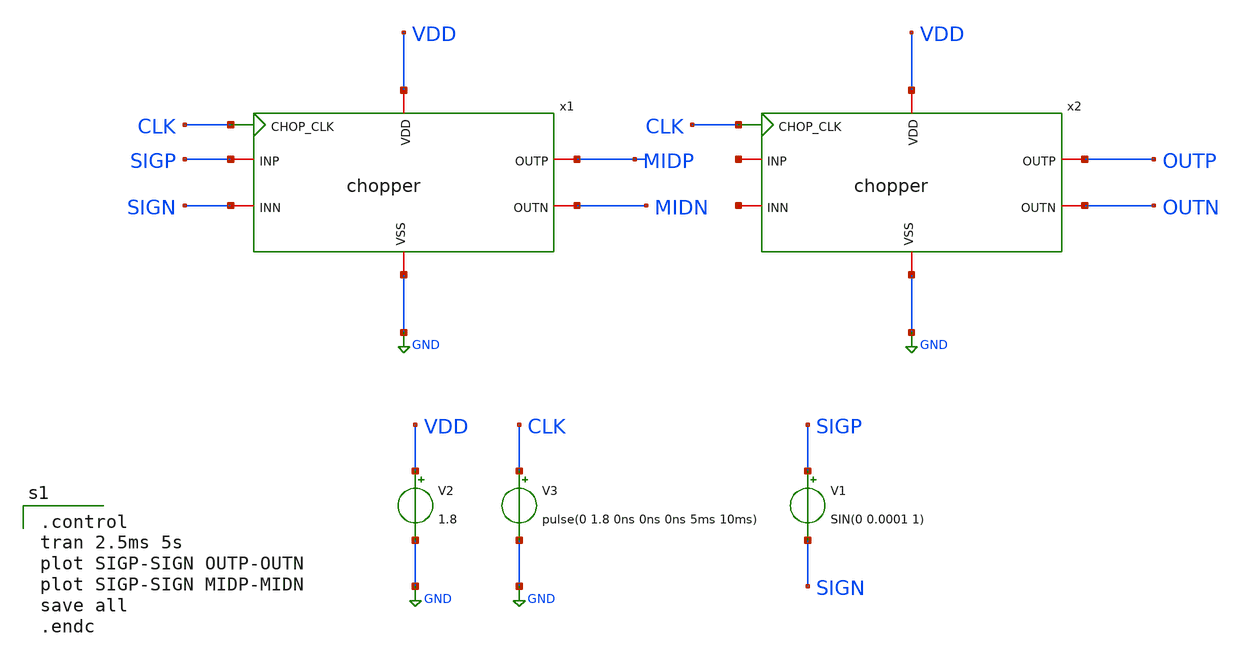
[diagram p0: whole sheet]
** sch_path: opamp_lna/chopper_tb.sch
**.subckt chopper_tb
x1 GND VDD MIDP SIGP CLK MIDN SIGN chopper
V1 SIGP SIGN SIN(0 0.0001 1)
V2 VDD GND 1.8
V3 CLK GND pulse(0 1.8 0ns 0ns 0ns 5ms 10ms)
x2 GND VDD OUTP net1 CLK OUTN net2 chopper
**** begin user architecture code

** opencircuitdesign pdks install
.lib $::SKYWATER_MODELS/sky130.lib.spice tt
.include $::SKYWATER_STDCELLS/sky130_fd_sc_hd.spice


.control
tran 2.5ms 5s
plot SIGP-SIGN OUTP-OUTN
plot SIGP-SIGN MIDP-MIDN
save all
.endc

**** end user architecture code
**.ends

* expanding   symbol:  chopper.sym # of pins=7
** sym_path: opamp_lna/chopper.sym
** sch_path: opamp_lna/chopper.sch
.subckt chopper VSS VDD OUTP INP CHOP_CLK OUTN INN
*.ipin CHOP_CLK
*.iopin INP
*.iopin INN
*.iopin OUTP
*.iopin OUTN
*.iopin VSS
*.iopin VDD
x5 CHOP_CLK VSS VNB VPB VDD net2 sky130_fd_sc_hd__clkbuf_2
x1 CHOP_CLK VGND VNB VPB VPWR net1 sky130_fd_sc_hd__clkinv_2
x2 net1 VSS VNB VPB VDD SWB sky130_fd_sc_hd__clkinv_8
x3 net2 VSS VNB VPB VDD SW sky130_fd_sc_hd__clkinv_8
XM5 INP SWB OUTN VSS sky130_fd_pr__nfet_01v8 L=0.15 W=1 nf=1 ad='int((nf+1)/2) * W/nf * 0.29' as='int((nf+2)/2) * W/nf * 0.29'
+ pd='2*int((nf+1)/2) * (W/nf + 0.29)' ps='2*int((nf+2)/2) * (W/nf + 0.29)' nrd='0.29 / W' nrs='0.29 / W'
+ sa=0 sb=0 sd=0 mult=1 m=1
XM6 OUTN SW INP VDD sky130_fd_pr__pfet_01v8 L=0.15 W=1 nf=1 ad='int((nf+1)/2) * W/nf * 0.29' as='int((nf+2)/2) * W/nf * 0.29'
+ pd='2*int((nf+1)/2) * (W/nf + 0.29)' ps='2*int((nf+2)/2) * (W/nf + 0.29)' nrd='0.29 / W' nrs='0.29 / W'
+ sa=0 sb=0 sd=0 mult=1 m=1
XM7 INP SW OUTP VSS sky130_fd_pr__nfet_01v8 L=0.15 W=8 nf=1 ad='int((nf+1)/2) * W/nf * 0.29' as='int((nf+2)/2) * W/nf * 0.29'
+ pd='2*int((nf+1)/2) * (W/nf + 0.29)' ps='2*int((nf+2)/2) * (W/nf + 0.29)' nrd='0.29 / W' nrs='0.29 / W'
+ sa=0 sb=0 sd=0 mult=1 m=1
XM8 OUTP SWB INP VDD sky130_fd_pr__pfet_01v8 L=0.15 W=8 nf=1 ad='int((nf+1)/2) * W/nf * 0.29' as='int((nf+2)/2) * W/nf * 0.29'
+ pd='2*int((nf+1)/2) * (W/nf + 0.29)' ps='2*int((nf+2)/2) * (W/nf + 0.29)' nrd='0.29 / W' nrs='0.29 / W'
+ sa=0 sb=0 sd=0 mult=1 m=1
XM9 INN SW OUTN VSS sky130_fd_pr__nfet_01v8 L=0.15 W=8 nf=1 ad='int((nf+1)/2) * W/nf * 0.29' as='int((nf+2)/2) * W/nf * 0.29'
+ pd='2*int((nf+1)/2) * (W/nf + 0.29)' ps='2*int((nf+2)/2) * (W/nf + 0.29)' nrd='0.29 / W' nrs='0.29 / W'
+ sa=0 sb=0 sd=0 mult=1 m=1
XM10 OUTN SWB INN VDD sky130_fd_pr__pfet_01v8 L=0.15 W=8 nf=1 ad='int((nf+1)/2) * W/nf * 0.29' as='int((nf+2)/2) * W/nf * 0.29'
+ pd='2*int((nf+1)/2) * (W/nf + 0.29)' ps='2*int((nf+2)/2) * (W/nf + 0.29)' nrd='0.29 / W' nrs='0.29 / W'
+ sa=0 sb=0 sd=0 mult=1 m=1
XM11 INN SWB OUTP VSS sky130_fd_pr__nfet_01v8 L=0.15 W=8 nf=1 ad='int((nf+1)/2) * W/nf * 0.29' as='int((nf+2)/2) * W/nf * 0.29'
+ pd='2*int((nf+1)/2) * (W/nf + 0.29)' ps='2*int((nf+2)/2) * (W/nf + 0.29)' nrd='0.29 / W' nrs='0.29 / W'
+ sa=0 sb=0 sd=0 mult=1 m=1
XM12 OUTP SW INN VDD sky130_fd_pr__pfet_01v8 L=0.15 W=8 nf=1 ad='int((nf+1)/2) * W/nf * 0.29' as='int((nf+2)/2) * W/nf * 0.29'
+ pd='2*int((nf+1)/2) * (W/nf + 0.29)' ps='2*int((nf+2)/2) * (W/nf + 0.29)' nrd='0.29 / W' nrs='0.29 / W'
+ sa=0 sb=0 sd=0 mult=1 m=1
.ends

.GLOBAL GND
.end
